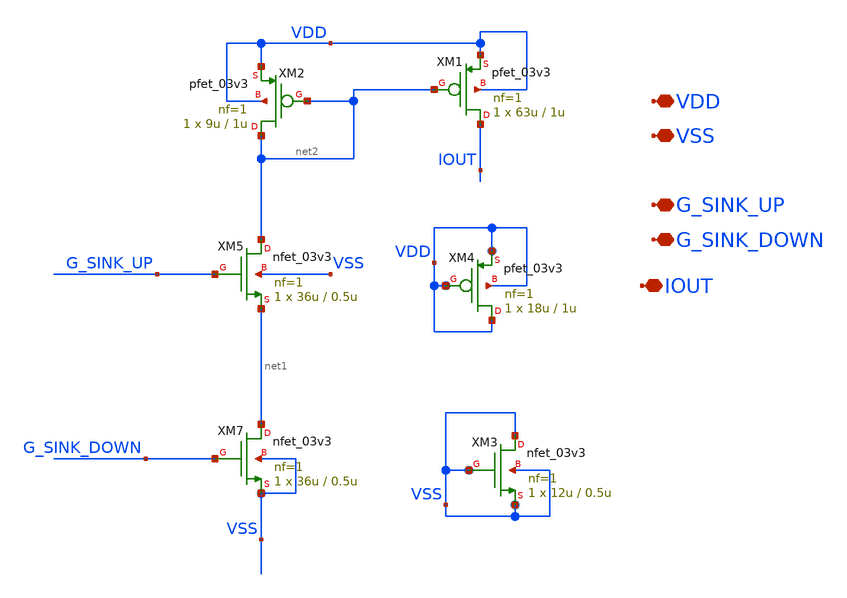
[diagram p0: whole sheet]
** sch_path: AWG_OUTPUT_AND_MUX_PAKISTAN_05/xschem/mioor_opamp_single.sch
**.subckt mioor_opamp_single VDD VSS G_SINK_UP G_SINK_DOWN IOUT
*.iopin VDD
*.iopin VSS
*.iopin G_SINK_UP
*.iopin G_SINK_DOWN
*.iopin IOUT
XM5 net2 G_SINK_UP net1 VSS nfet_03v3 L=0.5u W=36u nf=1 ad='int((nf+1)/2) * W/nf * 0.18u' as='int((nf+2)/2) * W/nf * 0.18u'
+ pd='2*int((nf+1)/2) * (W/nf + 0.18u)' ps='2*int((nf+2)/2) * (W/nf + 0.18u)' nrd='0.18u / W' nrs='0.18u / W'
+ sa=0 sb=0 sd=0 m=1
XM7 net1 G_SINK_DOWN VSS VSS nfet_03v3 L=0.5u W=36u nf=1 ad='int((nf+1)/2) * W/nf * 0.18u' as='int((nf+2)/2) * W/nf * 0.18u'
+ pd='2*int((nf+1)/2) * (W/nf + 0.18u)' ps='2*int((nf+2)/2) * (W/nf + 0.18u)' nrd='0.18u / W' nrs='0.18u / W'
+ sa=0 sb=0 sd=0 m=1
XM2 net2 net2 VDD VDD pfet_03v3 L=1u W=9u nf=1 ad='int((nf+1)/2) * W/nf * 0.18u' as='int((nf+2)/2) * W/nf * 0.18u'
+ pd='2*int((nf+1)/2) * (W/nf + 0.18u)' ps='2*int((nf+2)/2) * (W/nf + 0.18u)' nrd='0.18u / W' nrs='0.18u / W'
+ sa=0 sb=0 sd=0 m=1
XM1 IOUT net2 VDD VDD pfet_03v3 L=1u W=63u nf=1 ad='int((nf+1)/2) * W/nf * 0.18u' as='int((nf+2)/2) * W/nf * 0.18u'
+ pd='2*int((nf+1)/2) * (W/nf + 0.18u)' ps='2*int((nf+2)/2) * (W/nf + 0.18u)' nrd='0.18u / W' nrs='0.18u / W'
+ sa=0 sb=0 sd=0 m=1
XM3 VSS VSS VSS VSS nfet_03v3 L=0.5u W=12u nf=1 ad='int((nf+1)/2) * W/nf * 0.18u' as='int((nf+2)/2) * W/nf * 0.18u'
+ pd='2*int((nf+1)/2) * (W/nf + 0.18u)' ps='2*int((nf+2)/2) * (W/nf + 0.18u)' nrd='0.18u / W' nrs='0.18u / W'
+ sa=0 sb=0 sd=0 m=1
XM4 VDD VDD VDD VDD pfet_03v3 L=1u W=18u nf=1 ad='int((nf+1)/2) * W/nf * 0.18u' as='int((nf+2)/2) * W/nf * 0.18u'
+ pd='2*int((nf+1)/2) * (W/nf + 0.18u)' ps='2*int((nf+2)/2) * (W/nf + 0.18u)' nrd='0.18u / W' nrs='0.18u / W'
+ sa=0 sb=0 sd=0 m=1
**.ends
.end
